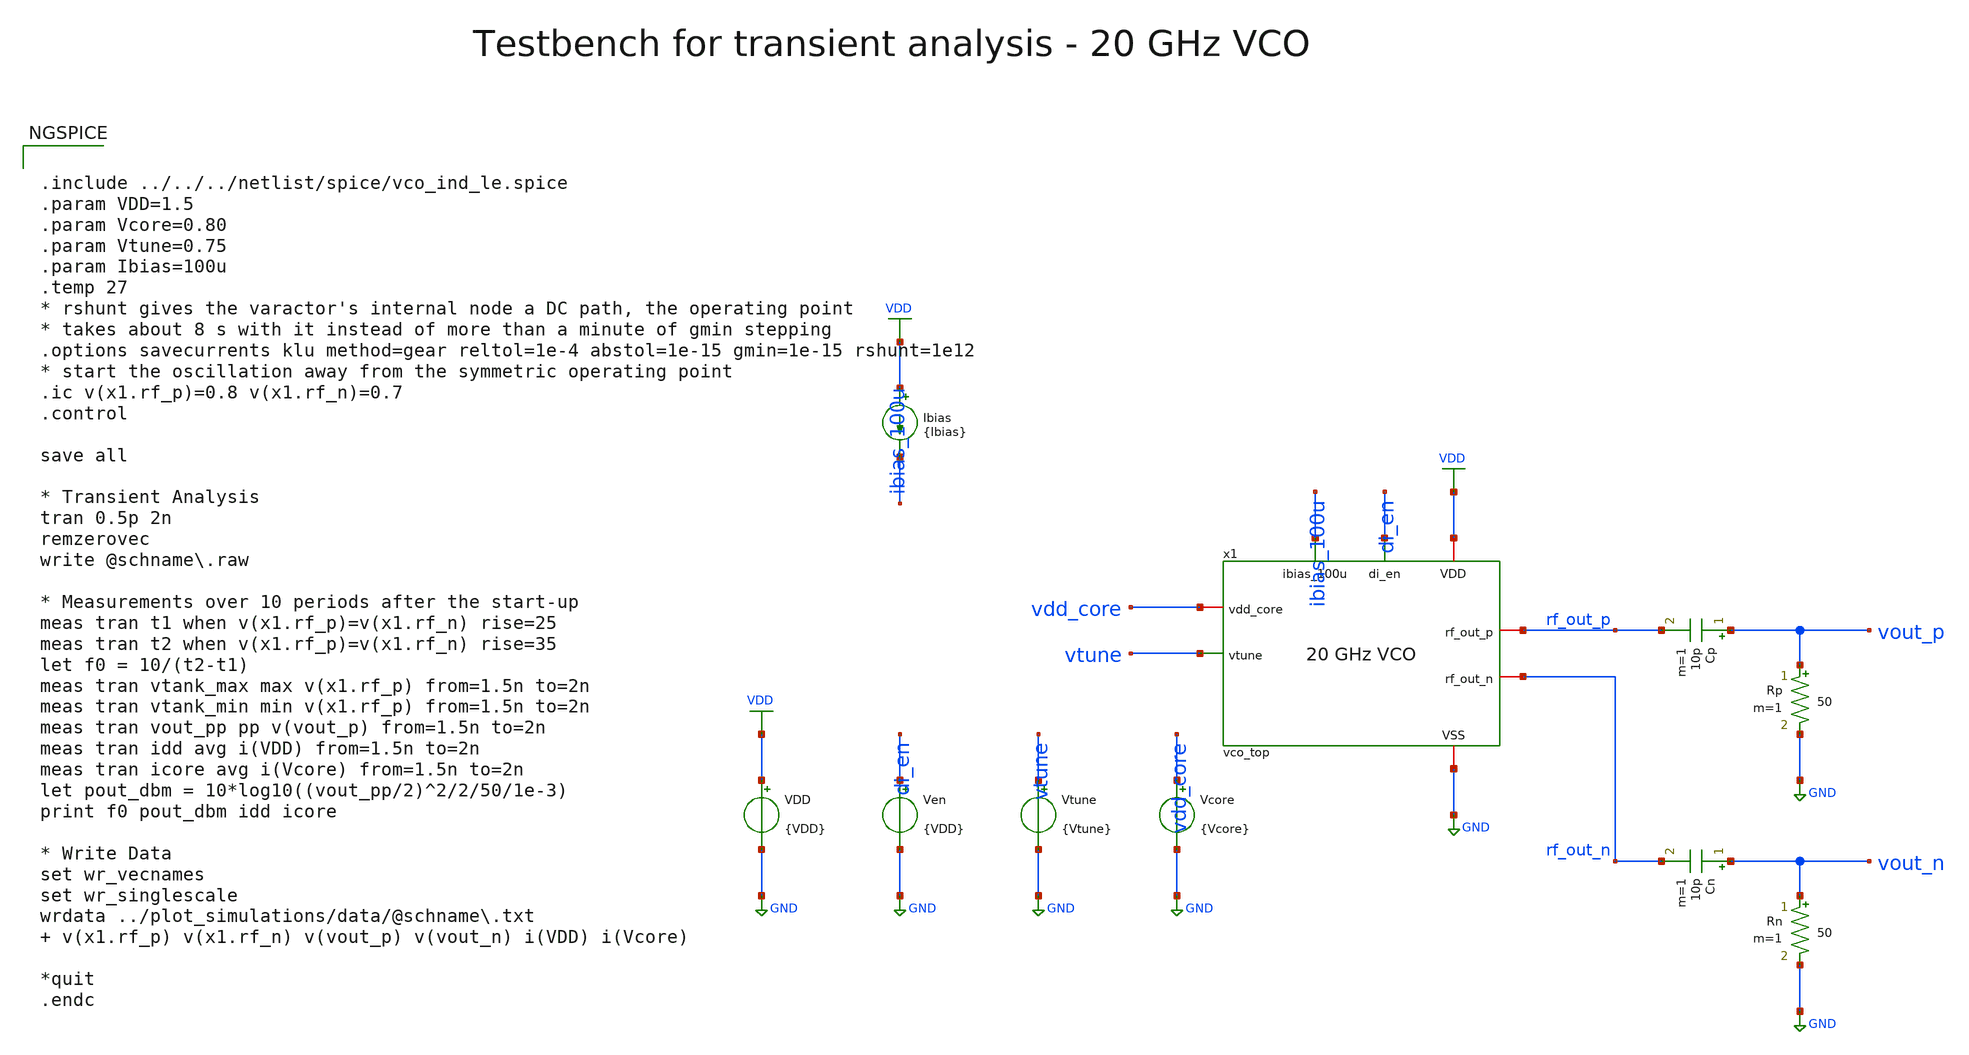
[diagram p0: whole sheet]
** sch_path: macros/vco/testbenches/xschem/vco_top_tb_tran.sch
**.subckt vco_top_tb_tran
x1 ibias_100u di_en VDD GND vdd_core vtune rf_out_p rf_out_n vco_top
Vcore vdd_core GND {Vcore}
Cp vout_p rf_out_p 10p m=1
Rp vout_p GND 50 m=1
Cn vout_n rf_out_n 10p m=1
Rn vout_n GND 50 m=1
VDD VDD GND {VDD}
Ven di_en GND {VDD}
Vtune vtune GND {Vtune}
Ibias VDD ibias_100u {Ibias}
**** begin user architecture code


.include ../../../netlist/spice/vco_ind_le.spice
.param VDD=1.5
.param Vcore=0.80
.param Vtune=0.75
.param Ibias=100u
.temp 27
* rshunt gives the varactor's internal node a DC path, the operating point
* takes about 8 s with it instead of more than a minute of gmin stepping
.options savecurrents klu method=gear reltol=1e-4 abstol=1e-15 gmin=1e-15 rshunt=1e12
* start the oscillation away from the symmetric operating point
.ic v(x1.rf_p)=0.8 v(x1.rf_n)=0.7
.control

save all

* Transient Analysis
tran 0.5p 2n
remzerovec
write @schname\.raw

* Measurements over 10 periods after the start-up
meas tran t1 when v(x1.rf_p)=v(x1.rf_n) rise=25
meas tran t2 when v(x1.rf_p)=v(x1.rf_n) rise=35
let f0 = 10/(t2-t1)
meas tran vtank_max max v(x1.rf_p) from=1.5n to=2n
meas tran vtank_min min v(x1.rf_p) from=1.5n to=2n
meas tran vout_pp pp v(vout_p) from=1.5n to=2n
meas tran idd avg i(VDD) from=1.5n to=2n
meas tran icore avg i(Vcore) from=1.5n to=2n
let pout_dbm = 10*log10((vout_pp/2)^2/2/50/1e-3)
print f0 pout_dbm idd icore

* Write Data
set wr_vecnames
set wr_singlescale
wrdata ../plot_simulations/data/@schname\.txt  v(x1.rf_p) v(x1.rf_n) v(vout_p) v(vout_n) i(VDD) i(Vcore)

*quit
.endc



.lib cornerMOSlv.lib mos_tt
.lib cornerMOShv.lib mos_tt
.lib cornerRES.lib res_typ
.lib cornerCAP.lib cap_typ

**** end user architecture code
**.ends

* expanding   symbol:  vco_top.sym # of pins=8
** sym_path: vco_top.sym
** sch_path: vco_top.sch
.subckt vco_top ibias_100u di_en VDD VSS vdd_core vtune rf_out_p rf_out_n
*.iopin VDD
*.iopin VSS
*.iopin vdd_core
*.ipin ibias_100u
*.ipin di_en
*.ipin vtune
*.iopin rf_out_p
*.iopin rf_out_n
xbias ibias_100u di_en VDD VSS vbg_buf vbn_buf vco_bias
xcore vdd_core VSS vtune rf_p rf_n vco_core
xbuf vbn_buf vbg_buf VDD VSS rf_p rf_n rf_out_p rf_out_n vco_buf
xind rf_p rf_n vdd_core vco_ind_le
.ends


* expanding   symbol:  vco_bias.sym # of pins=6
** sym_path: vco_bias.sym
** sch_path: vco_bias.sch
.subckt vco_bias ibias_100u di_en VDD VSS vbg_buf vbn_buf
*.iopin VDD
*.iopin VSS
*.ipin di_en
*.ipin ibias_100u
*.iopin vbn_buf
*.iopin vbg_buf
XMPi1 en_b di_en VDD VDD sg13_lv_pmos w=1u l=0.13u ng=1 m=1 mm_ok=1
XMNi1 en_b di_en VSS VSS sg13_lv_nmos w=0.5u l=0.13u ng=1 m=1 mm_ok=1
XMPi2 en en_b VDD VDD sg13_lv_pmos w=1u l=0.13u ng=1 m=1 mm_ok=1
XMNi2 en en_b VSS VSS sg13_lv_nmos w=0.5u l=0.13u ng=1 m=1 mm_ok=1
XMN0 ibias_100u ibias_100u VSS VSS sg13_lv_nmos w=2.5u l=0.5u ng=1 m=1 mm_ok=1
XMNd0 ibias_100u en_b VSS VSS sg13_lv_nmos w=1u l=0.13u ng=1 m=1 mm_ok=1
XRn ibias_100u vbn_buf VSS rhigh w=0.5e-6 l=32e-6 m=1 b=0 mm_ok=1
XMNd1 vbn_buf en_b VSS VSS sg13_lv_nmos w=1u l=0.13u ng=1 m=1 mm_ok=1
XMN1 vbp_ref ibias_100u VSS VSS sg13_lv_nmos w=2.5u l=0.5u ng=1 m=1 mm_ok=1
XMP1 vbp_ref vbp_ref VDD VDD sg13_lv_pmos w=5u l=0.5u ng=1 m=1 mm_ok=1
XMPd vbp_ref en VDD VDD sg13_lv_pmos w=1u l=0.13u ng=1 m=1 mm_ok=1
XMP2 vbg_int vbp_ref VDD VDD sg13_lv_pmos w=5u l=0.5u ng=1 m=1 mm_ok=1
XRg vbg_int nbg VSS rppd w=0.5e-6 l=8.5e-6 m=1 b=0 mm_ok=1
XMN3 nbg nbg VSS VSS sg13_lv_nmos w=2.5u l=0.5u ng=1 m=1 mm_ok=1
XMCn1 VSS vbn_buf VSS VSS sg13_lv_nmos w=40u l=10u ng=5 m=1 mm_ok=1
XMCn2 VSS vbn_buf VSS VSS sg13_lv_nmos w=40u l=10u ng=5 m=1 mm_ok=1
XRf vbg_int vbg_buf VSS rhigh w=0.5e-6 l=32e-6 m=1 b=0 mm_ok=1
XMCg1 VSS vbg_buf VSS VSS sg13_lv_nmos w=40u l=10u ng=5 m=1 mm_ok=1
XMCg2 VSS vbg_buf VSS VSS sg13_lv_nmos w=40u l=10u ng=5 m=1 mm_ok=1
.ends


* expanding   symbol:  vco_core.sym # of pins=5
** sym_path: vco_core.sym
** sch_path: vco_core.sch
.subckt vco_core vdd_core VSS vtune rf_p rf_n
*.iopin vdd_core
*.iopin VSS
*.ipin vtune
*.iopin rf_p
*.iopin rf_n
XCct1a1 vdd_core VSS cap_cmomf w=19e-6 l=26e-6 mmin=1 mmax=4 subblock=0 rfmodel=0 subscale=1 m=1 mm_ok=1
XCct1a2 vdd_core VSS cap_cmomf w=19e-6 l=26e-6 mmin=1 mmax=4 subblock=0 rfmodel=0 subscale=1 m=1 mm_ok=1
xvar rf_p rf_n vtune VSS vco_var
XM1 rf_p rf_n VSS VSS sg13_lv_nmos w=20u l=0.13u ng=10 m=1 mm_ok=1
XM2 rf_n rf_p VSS VSS sg13_lv_nmos w=20u l=0.13u ng=10 m=1 mm_ok=1
XCct2a vdd_core VSS cap_cmomf w=25.5e-6 l=19e-6 mmin=1 mmax=4 subblock=0 rfmodel=0 subscale=1 m=1 mm_ok=1
XCct1b1 VSS vdd_core cap_cmomf w=19e-6 l=26e-6 mmin=1 mmax=4 subblock=0 rfmodel=0 subscale=1 m=1 mm_ok=1
XCct1b2 VSS vdd_core cap_cmomf w=19e-6 l=26e-6 mmin=1 mmax=4 subblock=0 rfmodel=0 subscale=1 m=1 mm_ok=1
XCct2b VSS vdd_core cap_cmomf w=25.5e-6 l=19e-6 mmin=1 mmax=4 subblock=0 rfmodel=0 subscale=1 m=1 mm_ok=1
.ends


* expanding   symbol:  vco_buf.sym # of pins=8
** sym_path: vco_buf.sym
** sch_path: vco_buf.sch
.subckt vco_buf vbn_buf vbg_buf VDD VSS rf_p rf_n rf_out_p rf_out_n
*.iopin VDD
*.iopin VSS
*.iopin rf_out_n
*.iopin rf_out_p
*.ipin vbn_buf
*.iopin rf_p
*.iopin rf_n
*.ipin vbg_buf
XMB1 rf_out_n gp tail VSS sg13_lv_nmos w=24u l=0.13u ng=12 m=1 mm_ok=1
XMB2 rf_out_p gn tail VSS sg13_lv_nmos w=24u l=0.13u ng=12 m=1 mm_ok=1
XRL1 VDD rf_out_n VSS rppd w=10e-6 l=1.65e-6 m=1 b=0 mm_ok=1
XRL2 VDD rf_out_p VSS rppd w=10e-6 l=1.65e-6 m=1 b=0 mm_ok=1
XMBt tail vbn_buf VSS VSS sg13_lv_nmos w=150u l=0.5u ng=30 m=1 mm_ok=1
XCc1 gp rf_p cap_cmomf w=10e-6 l=18.6e-6 mmin=2 mmax=4 subblock=0 rfmodel=0 subscale=1 m=1 mm_ok=1
XCc2 gn rf_n cap_cmomf w=10e-6 l=18.6e-6 mmin=2 mmax=4 subblock=0 rfmodel=0 subscale=1 m=1 mm_ok=1
XRb1 vbg_buf gp VSS rhigh w=0.5e-6 l=8e-6 m=1 b=0 mm_ok=1
XRb2 vbg_buf gn VSS rhigh w=0.5e-6 l=8e-6 m=1 b=0 mm_ok=1
.ends


* expanding   symbol:  vco_var.sym # of pins=4
** sym_path: vco_var.sym
** sch_path: vco_var.sch
.subckt vco_var rf_p rf_n vtune VSS
*.ipin vtune
*.iopin rf_p
*.iopin rf_n
*.iopin VSS
XCvar1 rf_p vtune rf_n VSS sg13_hv_svaricap w=3.74u l=0.3u Nx=8 mm_ok=1
XCvar2 rf_p vtune rf_n VSS sg13_hv_svaricap w=3.74u l=0.3u Nx=8 mm_ok=1
XCvar3 rf_p vtune rf_n VSS sg13_hv_svaricap w=3.74u l=0.3u Nx=8 mm_ok=1
.ends

.GLOBAL VDD
.GLOBAL GND
.end
